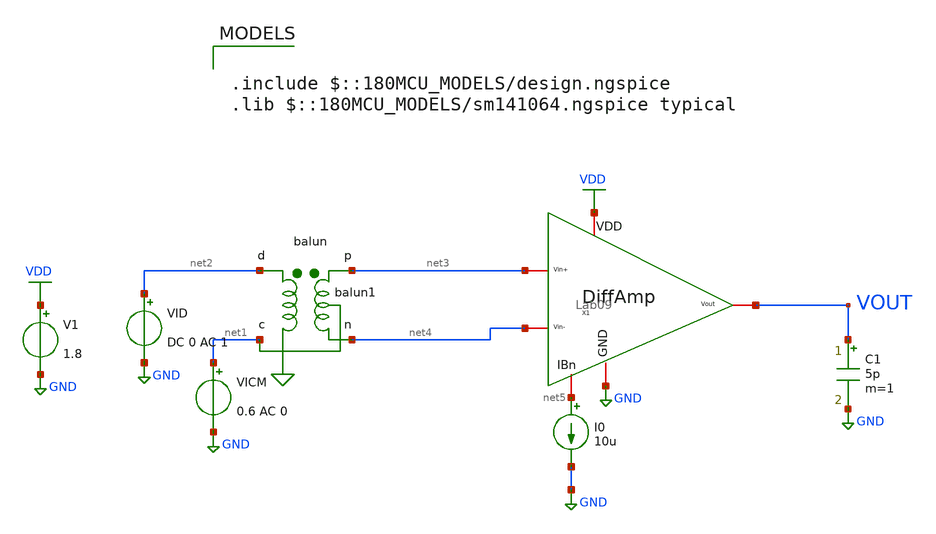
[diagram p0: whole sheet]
** sch_path: ITI_Labs/Lab9_Xschem/Design/Lab09_tb.sch
**.subckt Lab09_tb
X1 VDD net5 net3 net4 VOUT GND Lab09
Xbalun1 net2 net1 net3 net4 balun
V1 VDD GND 1.8
I0 net5 GND 10u
VICM net1 GND 0.6 AC 0
VID net2 GND DC 0 AC 1
C1 VOUT GND 5p m=1
**** begin user architecture code


.include sim_script.sim



.include $::180MCU_MODELS/design.ngspice
.lib $::180MCU_MODELS/sm141064.ngspice typical

**** end user architecture code
**.ends
.GLOBAL VDD
.GLOBAL GND
.end
